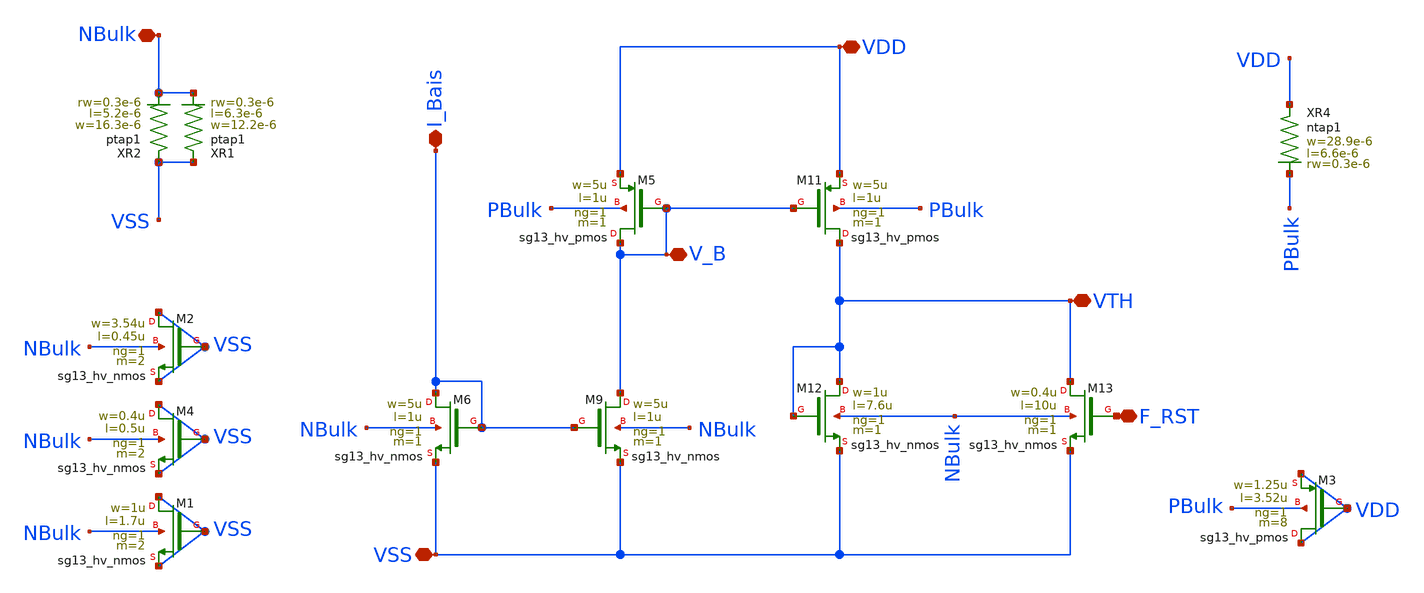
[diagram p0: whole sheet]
** sch_path: LVS/LVS_Sch/Divider.sch
**.subckt Divider VDD NBulk VSS I_Bais VTH F_RST V_B
*.iopin VDD
*.iopin NBulk
*.iopin VSS
*.iopin I_Bais
*.iopin VTH
*.iopin F_RST
*.iopin V_B
XR2 VSS NBulk ptap1 R=5.452 w=16.3e-6 l=5.2e-6 rw=0.3e-6
XR4 VDD PBulk ntap1 R=3.265 w=28.9e-6 l=6.6e-6 rw=0.3e-6
XM3 VDD VDD VDD PBulk sg13_hv_pmos w=1.25u l=3.52u ng=1 m=8 mm_ok=1
XM4 VSS VSS VSS NBulk sg13_hv_nmos w=0.4u l=0.5u ng=1 m=2 mm_ok=1
XM5 V_B V_B VDD PBulk sg13_hv_pmos w=5u l=1u ng=1 m=1 mm_ok=1
XM9 V_B I_Bais VSS NBulk sg13_hv_nmos w=5u l=1u ng=1 m=1 mm_ok=1
XM11 VTH V_B VDD PBulk sg13_hv_pmos w=5u l=1u ng=1 m=1 mm_ok=1
XM12 VTH VTH VSS NBulk sg13_hv_nmos w=1u l=7.6u ng=1 m=1 mm_ok=1
XM13 VTH F_RST VSS NBulk sg13_hv_nmos w=0.4u l=10u ng=1 m=1 mm_ok=1
XR1 VSS NBulk ptap1 R=6.366 w=12.2e-6 l=6.3e-6 rw=0.3e-6
XM1 VSS VSS VSS NBulk sg13_hv_nmos w=1u l=1.7u ng=1 m=2 mm_ok=1
XM2 VSS VSS VSS NBulk sg13_hv_nmos w=3.54u l=0.45u ng=1 m=2 mm_ok=1
XM6 I_Bais I_Bais VSS NBulk sg13_hv_nmos w=5u l=1u ng=1 m=1 mm_ok=1
**.ends
.end
